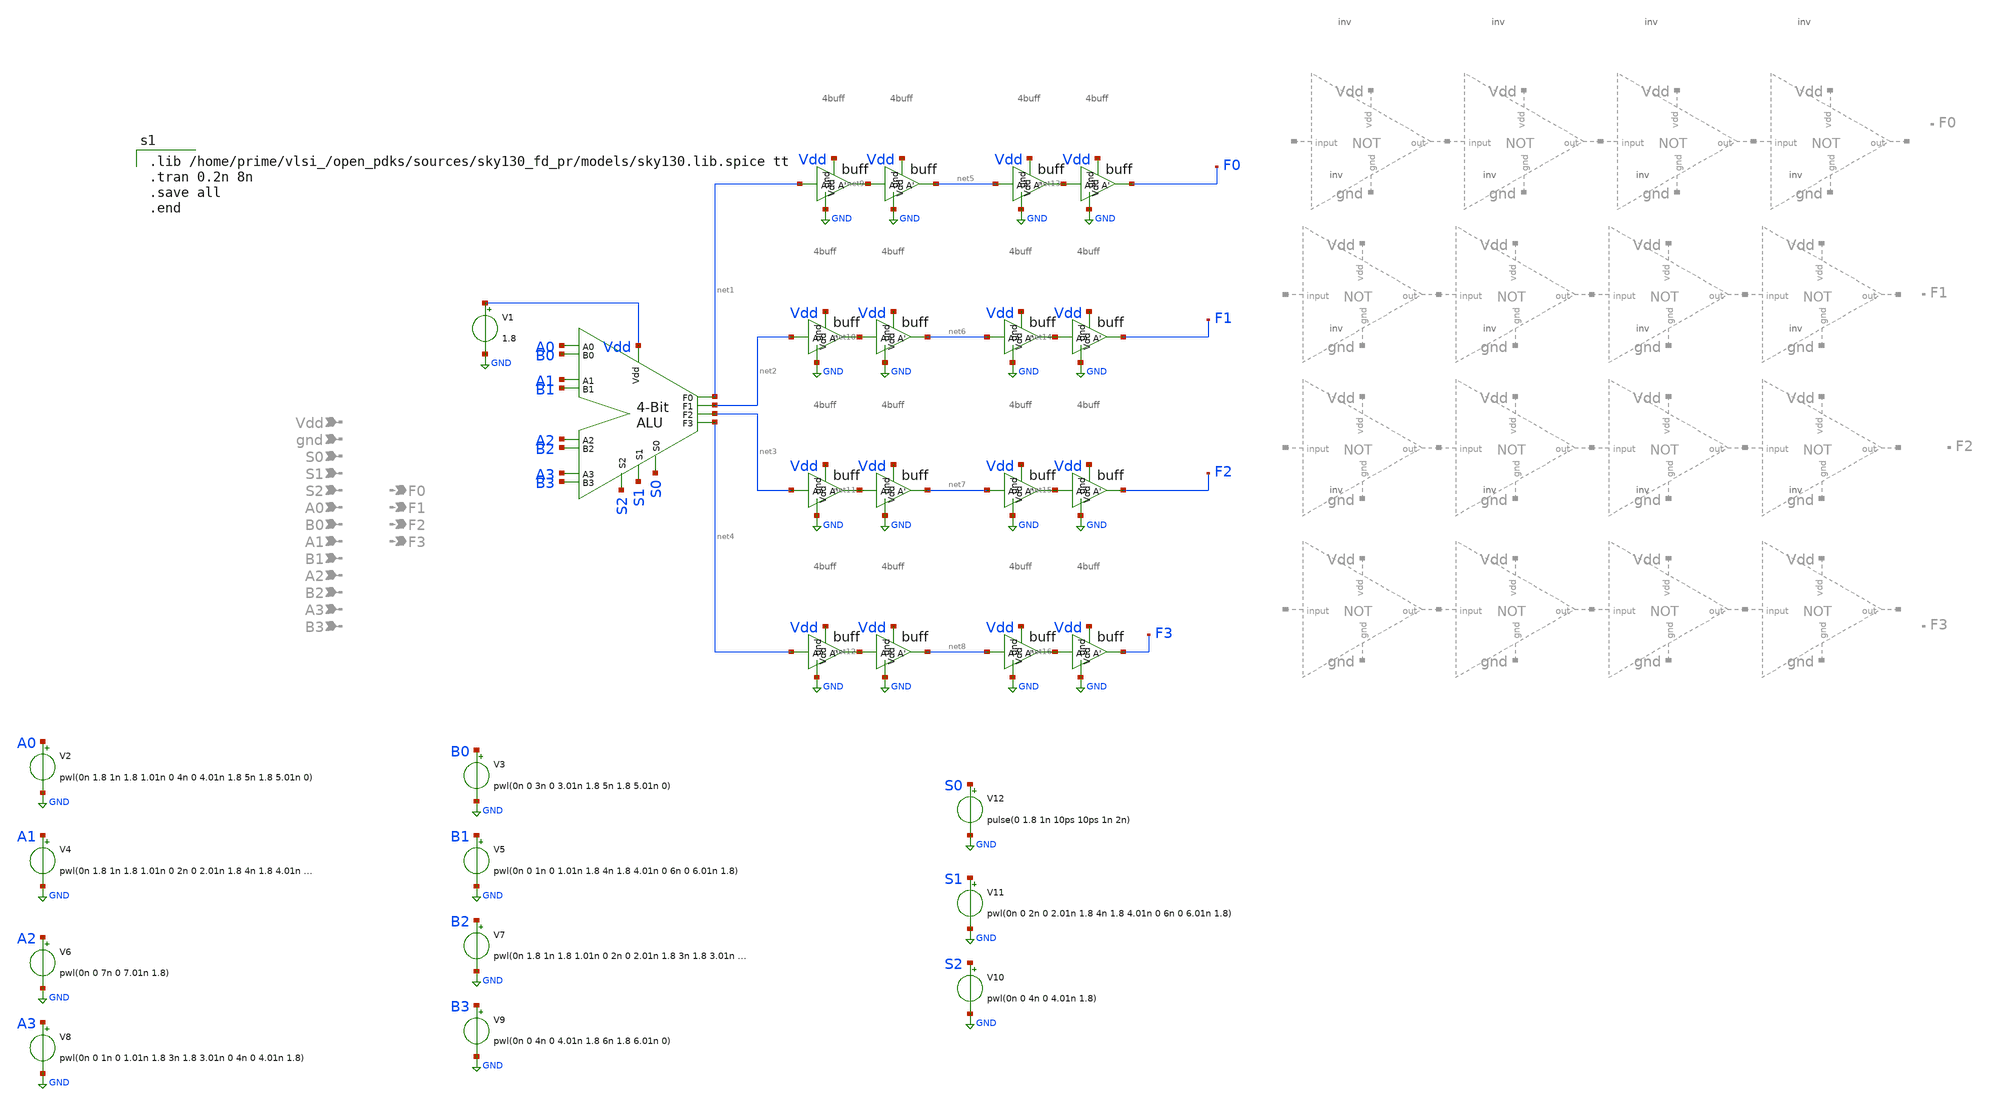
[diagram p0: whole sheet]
** sch_path: extra_stuff/top.sch
**.subckt top
x1 net1 net2 net3 net4 Vdd A0 B0 A1 B1 A2 B2 A3 B3 S0 S1 S2 alu
V2 A0 GND pwl(0n 1.8 1n 1.8 1.01n 0 4n 0 4.01n 1.8 5n 1.8 5.01n 0)
V3 B0 GND pwl(0n 0 3n 0 3.01n 1.8 5n 1.8 5.01n 0)
V4 A1 GND pwl(0n 1.8 1n 1.8 1.01n 0 2n 0 2.01n 1.8 4n 1.8 4.01n 0 6n 0 6.01n 1.8 7n 1.8 7.01n 0)
V5 B1 GND pwl(0n 0 1n 0 1.01n 1.8 4n 1.8 4.01n 0 6n 0 6.01n 1.8)
V6 A2 GND pwl(0n 0 7n 0 7.01n 1.8)
V7 B2 GND pwl(0n 1.8 1n 1.8 1.01n 0 2n 0 2.01n 1.8 3n 1.8 3.01n 0 4n 0 4.01n 1.8 5n 1.8 5.01n 0 6n 0
+ 6.01n 1.8)
V8 A3 GND pwl(0n 0 1n 0 1.01n 1.8 3n 1.8 3.01n 0 4n 0 4.01n 1.8)
V9 B3 GND pwl(0n 0 4n 0 4.01n 1.8 6n 1.8 6.01n 0)
V10 S2 GND pwl(0n 0 4n 0 4.01n 1.8)
V11 S1 GND pwl(0n 0 2n 0 2.01n 1.8 4n 1.8 4.01n 0 6n 0 6.01n 1.8)
V12 S0 GND pulse(0 1.8 1n 10ps 10ps 1n 2n)
V1 Vdd GND 1.8
x2 net9 GND net1 Vdd 4buff
x3 net5 GND net9 Vdd 4buff
x6 net10 GND net2 Vdd 4buff
x7 net6 GND net10 Vdd 4buff
x16 net11 GND net3 Vdd 4buff
x17 net7 GND net11 Vdd 4buff
x20 net12 GND net4 Vdd 4buff
x21 net8 GND net12 Vdd 4buff
x4 net13 GND net5 Vdd 4buff
x5 F0 GND net13 Vdd 4buff
x34 net14 GND net6 Vdd 4buff
x35 F1 GND net14 Vdd 4buff
x39 net15 GND net7 Vdd 4buff
x40 F2 GND net15 Vdd 4buff
x22 net16 GND net8 Vdd 4buff
x23 F3 GND net16 Vdd 4buff
**** begin user architecture code

.lib /home/prime/vlsi_/open_pdks/sources/sky130_fd_pr/models/sky130.lib.spice tt
.tran 0.2n 8n
.save all
.end

**** end user architecture code
**.ends
.GLOBAL GND
.end
